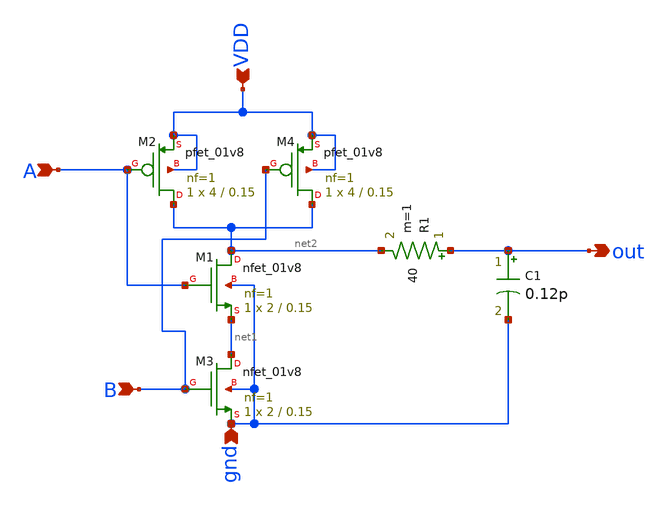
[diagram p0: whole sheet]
** sch_path: Logic_gates_using_cmos/Nand_Cmos.sch
**.subckt Nand_Cmos B A VDD gnd out
*.ipin B
*.ipin A
*.ipin VDD
*.ipin gnd
*.opin out
XM2 net2 A VDD VDD sky130_fd_pr__pfet_01v8 L=0.15 W=4 nf=1 ad='int((nf+1)/2) * W/nf * 0.29' as='int((nf+2)/2) * W/nf * 0.29'
+ pd='2*int((nf+1)/2) * (W/nf + 0.29)' ps='2*int((nf+2)/2) * (W/nf + 0.29)' nrd='0.29 / W' nrs='0.29 / W'
+ sa=0 sb=0 sd=0 mult=1 m=1
XM1 net2 A net1 gnd sky130_fd_pr__nfet_01v8 L=0.15 W=2 nf=1 ad='int((nf+1)/2) * W/nf * 0.29' as='int((nf+2)/2) * W/nf * 0.29'
+ pd='2*int((nf+1)/2) * (W/nf + 0.29)' ps='2*int((nf+2)/2) * (W/nf + 0.29)' nrd='0.29 / W' nrs='0.29 / W'
+ sa=0 sb=0 sd=0 mult=1 m=1
XM3 net1 B gnd gnd sky130_fd_pr__nfet_01v8 L=0.15 W=2 nf=1 ad='int((nf+1)/2) * W/nf * 0.29' as='int((nf+2)/2) * W/nf * 0.29'
+ pd='2*int((nf+1)/2) * (W/nf + 0.29)' ps='2*int((nf+2)/2) * (W/nf + 0.29)' nrd='0.29 / W' nrs='0.29 / W'
+ sa=0 sb=0 sd=0 mult=1 m=1
XM4 net2 B VDD VDD sky130_fd_pr__pfet_01v8 L=0.15 W=4 nf=1 ad='int((nf+1)/2) * W/nf * 0.29' as='int((nf+2)/2) * W/nf * 0.29'
+ pd='2*int((nf+1)/2) * (W/nf + 0.29)' ps='2*int((nf+2)/2) * (W/nf + 0.29)' nrd='0.29 / W' nrs='0.29 / W'
+ sa=0 sb=0 sd=0 mult=1 m=1
C1 out gnd 0.12p m=1
R1 out net2 40 m=1
**.ends
.end
